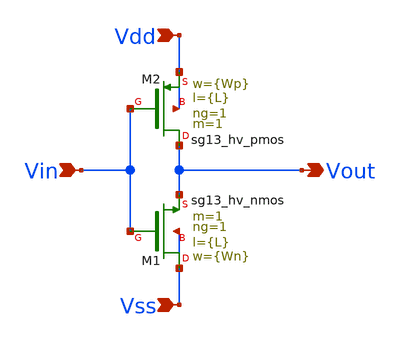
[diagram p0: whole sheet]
** sch_path: Taller1/Insumos/inv_hv.sch
**.subckt inv_hv Vin Vdd Vss Vout
*.ipin Vin
*.ipin Vdd
*.ipin Vss
*.opin Vout
XM1 Vss Vin Vout Vss sg13_hv_nmos w={Wn} l={L} ng=1 m=1 mm_ok=1
XM2 Vout Vin Vdd Vdd sg13_hv_pmos w={Wp} l={L} ng=1 m=1 mm_ok=1
**.ends
.end
